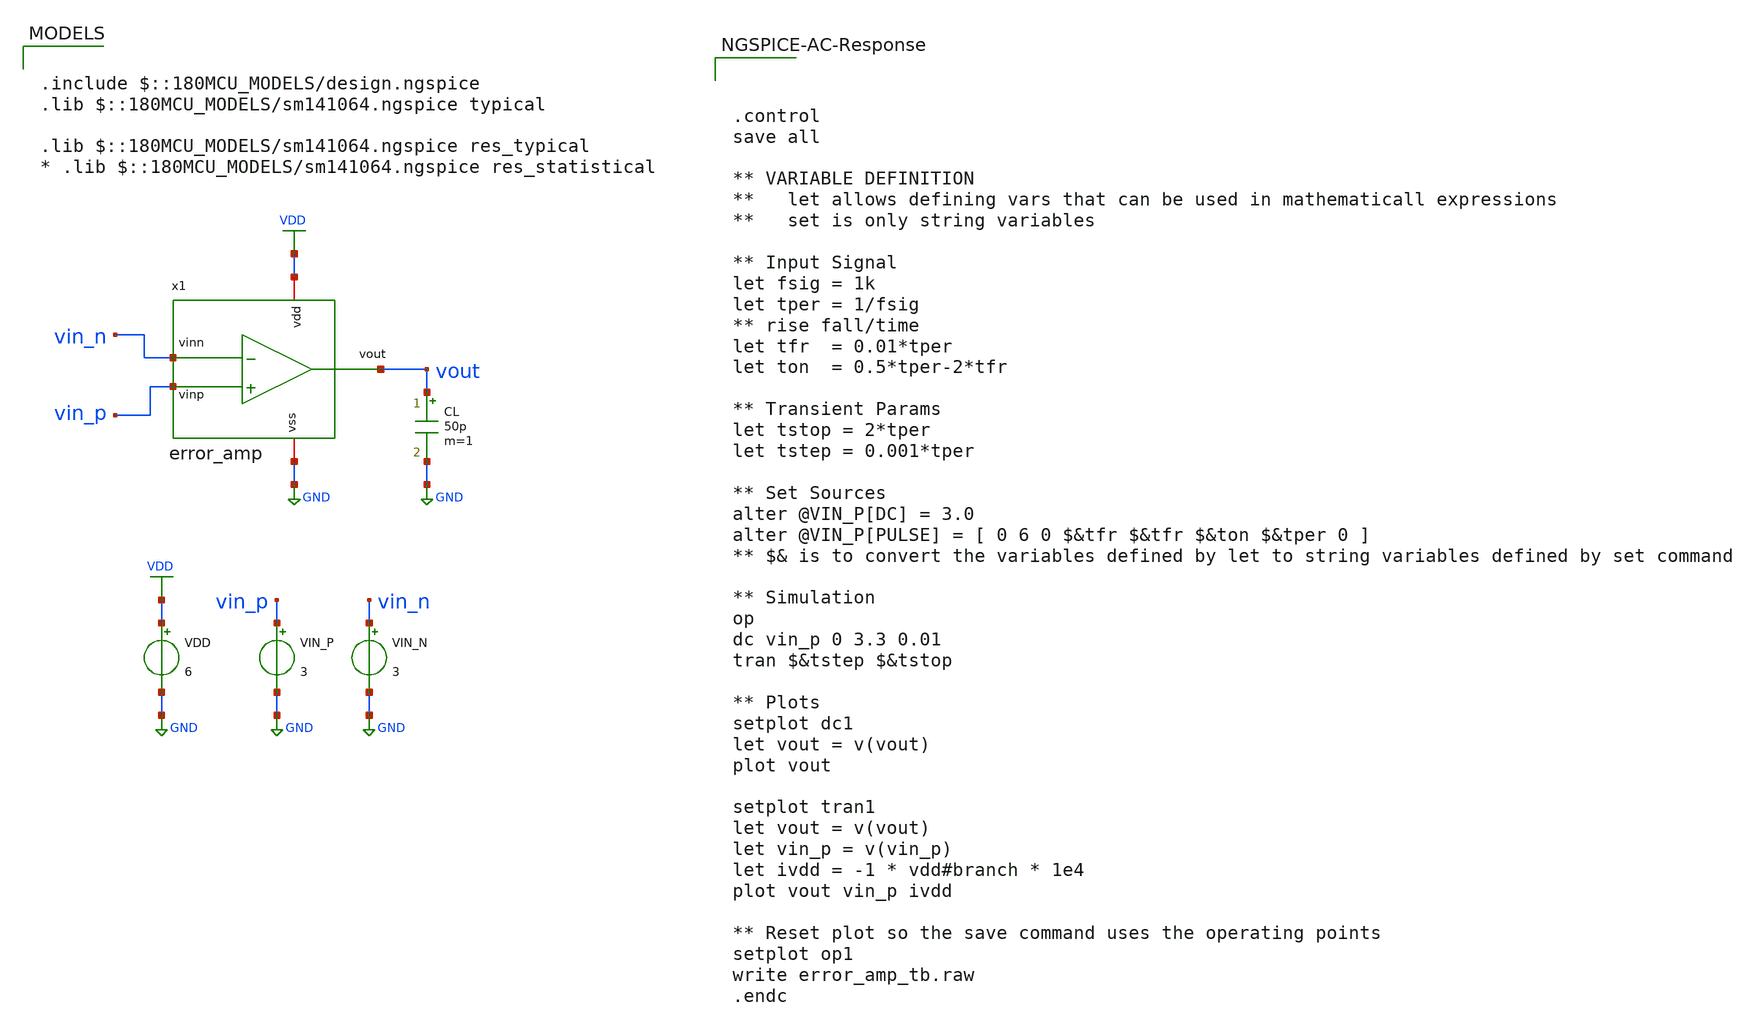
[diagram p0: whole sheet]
** sch_path: analog-db/drawings/ldo-005-ti-ldo-buffer-ref/gf180/error_amp/error_amp_tb.sch
**.subckt error_amp_tb
VDD VDD GND 6
VIN_P vin_p GND 3
VIN_N vin_n GND 3
CL vout GND 50p m=1
x1 VDD vout vin_p vin_n GND error_amp
**** begin user architecture code

.include $::180MCU_MODELS/design.ngspice
.lib $::180MCU_MODELS/sm141064.ngspice typical

.lib $::180MCU_MODELS/sm141064.ngspice res_typical
* .lib $::180MCU_MODELS/sm141064.ngspice res_statistical




.control
save all

** VARIABLE DEFINITION
**   let allows defining vars that can be used in mathematicall expressions
**   set is only string variables

** Input Signal
let fsig = 1k
let tper = 1/fsig
** rise fall/time
let tfr  = 0.01*tper
let ton  = 0.5*tper-2*tfr

** Transient Params
let tstop = 2*tper
let tstep = 0.001*tper

** Set Sources
alter @VIN_P[DC] = 3.0
alter @VIN_P[PULSE] = [ 0 6 0 $&tfr $&tfr $&ton $&tper 0 ]
** $& is to convert the variables defined by let to string variables defined by set command

** Simulation
op
dc vin_p 0 3.3 0.01
tran $&tstep $&tstop

** Plots
setplot dc1
let vout = v(vout)
plot vout

setplot tran1
let vout = v(vout)
let vin_p = v(vin_p)
let ivdd = -1 * vdd#branch * 1e4
plot vout vin_p ivdd

** Reset plot so the save command uses the operating points
setplot op1
write error_amp_tb.raw
.endc





.control
save all

** VARIABLE DEFINITION
**   let allows defining vars that can be used in mathematicall expressions
**   set is only string variables

** Input Signal
let fsig = 1k
let tper = 1/fsig
** rise fall/time
let tfr  = 0.01*tper
let ton  = 0.5*tper-2*tfr

** Transient Params
let tstop = 2*tper
let tstep = 0.001*tper

** Set Sources
alter @VIN_P[DC] = 3.0
alter @VIN_P[PULSE] = [ 0 6 0 $&tfr $&tfr $&ton $&tper 0 ]
** $& is to convert the variables defined by let to string variables defined by set command

** Simulation
op
dc vin_p 0 3.3 0.01
tran $&tstep $&tstop

** Plots
setplot dc1
let vout = v(vout)
plot vout

setplot tran1
let vout = v(vout)
let vin_p = v(vin_p)
let ivdd = -1 * vdd#branch * 1e4
plot vout vin_p ivdd

** Reset plot so the save command uses the operating points
setplot op1
write error_amp_tb.raw
.endc


**** end user architecture code
**.ends

* expanding   symbol:  ldo-005-ti-ldo-buffer-ref/gf180/error_amp/error_amp.sym # of pins=5
** sym_path: analog-db/circuits/amp_032_ti_ldo_error_selfbias/pdk/gf180mcu/schematic/error_amp.sym
** sch_path: analog-db/circuits/amp_032_ti_ldo_error_selfbias/pdk/gf180mcu/schematic/error_amp.sch
.subckt error_amp vdd vout vinp vinn vss
*.iopin vdd
*.iopin vss
*.ipin vinp
*.opin vout
*.ipin vinn
XM2 net_b vinp net_c vss nfet_06v0 L=0.7u W=68.542u nf=1 ad='int((nf+1)/2) * W/nf * 0.18u' as='int((nf+2)/2) * W/nf * 0.18u'
+ pd='2*int((nf+1)/2) * (W/nf + 0.18u)' ps='2*int((nf+2)/2) * (W/nf + 0.18u)' nrd='0.18u / W' nrs='0.18u / W'
+ sa=0 sb=0 sd=0 m=1
XM3m net_a net_d vdd vdd pfet_06v0 L=0.5u W=69.545u nf=1 ad='int((nf+1)/2) * W/nf * 0.18u' as='int((nf+2)/2) * W/nf * 0.18u'
+ pd='2*int((nf+1)/2) * (W/nf + 0.18u)' ps='2*int((nf+2)/2) * (W/nf + 0.18u)' nrd='0.18u / W' nrs='0.18u / W'
+ sa=0 sb=0 sd=0 m=1
XM4 net_f net_a net_d vdd pfet_06v0 L=0.5u W=10u nf=1 ad='int((nf+1)/2) * W/nf * 0.18u' as='int((nf+2)/2) * W/nf * 0.18u'
+ pd='2*int((nf+1)/2) * (W/nf + 0.18u)' ps='2*int((nf+2)/2) * (W/nf + 0.18u)' nrd='0.18u / W' nrs='0.18u / W'
+ sa=0 sb=0 sd=0 m=1
XM5 net_b net_d vdd vdd pfet_06v0 L=0.5u W=69.545u nf=1 ad='int((nf+1)/2) * W/nf * 0.18u' as='int((nf+2)/2) * W/nf * 0.18u'
+ pd='2*int((nf+1)/2) * (W/nf + 0.18u)' ps='2*int((nf+2)/2) * (W/nf + 0.18u)' nrd='0.18u / W' nrs='0.18u / W'
+ sa=0 sb=0 sd=0 m=1
XM6 vout net_b vdd vdd pfet_06v0 L=3.8349u W=20u nf=1 ad='int((nf+1)/2) * W/nf * 0.18u' as='int((nf+2)/2) * W/nf * 0.18u'
+ pd='2*int((nf+1)/2) * (W/nf + 0.18u)' ps='2*int((nf+2)/2) * (W/nf + 0.18u)' nrd='0.18u / W' nrs='0.18u / W'
+ sa=0 sb=0 sd=0 m=1
Cc net1 vout 6.7168p m=1
XRZ net_b net1 vdd ppolyf_u_3k r_width=1u r_length=9.476u m=1
XM1 net_a vinn net_c vss nfet_06v0 L=0.7u W=68.542u nf=1 ad='int((nf+1)/2) * W/nf * 0.18u' as='int((nf+2)/2) * W/nf * 0.18u'
+ pd='2*int((nf+1)/2) * (W/nf + 0.18u)' ps='2*int((nf+2)/2) * (W/nf + 0.18u)' nrd='0.18u / W' nrs='0.18u / W'
+ sa=0 sb=0 sd=0 m=1
XM_mirror_error_amp_ref net2 net2 vss vss nfet_06v0 L=2u W=34.533u nf=1 ad='int((nf+1)/2) * W/nf * 0.18u'
+ as='int((nf+2)/2) * W/nf * 0.18u' pd='2*int((nf+1)/2) * (W/nf + 0.18u)' ps='2*int((nf+2)/2) * (W/nf + 0.18u)'
+ nrd='0.18u / W' nrs='0.18u / W' sa=0 sb=0 sd=0 m=1
XM_mirror_f net_f net2 vss vss nfet_06v0 L=2u W=5u nf=1 ad='int((nf+1)/2) * W/nf * 0.18u' as='int((nf+2)/2) * W/nf * 0.18u'
+ pd='2*int((nf+1)/2) * (W/nf + 0.18u)' ps='2*int((nf+2)/2) * (W/nf + 0.18u)' nrd='0.18u / W' nrs='0.18u / W'
+ sa=0 sb=0 sd=0 m=1
XM_mirror_c net_c net2 vss vss nfet_06v0 L=2u W=34.533u nf=1 ad='int((nf+1)/2) * W/nf * 0.18u' as='int((nf+2)/2) * W/nf * 0.18u'
+ pd='2*int((nf+1)/2) * (W/nf + 0.18u)' ps='2*int((nf+2)/2) * (W/nf + 0.18u)' nrd='0.18u / W' nrs='0.18u / W'
+ sa=0 sb=0 sd=0 m=1
XM_mirror_ea_out vout net2 vss vss nfet_06v0 L=2u W=34.533u nf=1 ad='int((nf+1)/2) * W/nf * 0.18u' as='int((nf+2)/2) * W/nf * 0.18u'
+ pd='2*int((nf+1)/2) * (W/nf + 0.18u)' ps='2*int((nf+2)/2) * (W/nf + 0.18u)' nrd='0.18u / W' nrs='0.18u / W'
+ sa=0 sb=0 sd=0 m=1
XM_bias net2 net2 vdd vdd pfet_06v0 L=2u W=6.3111u nf=1 ad='int((nf+1)/2) * W/nf * 0.18u' as='int((nf+2)/2) * W/nf * 0.18u'
+ pd='2*int((nf+1)/2) * (W/nf + 0.18u)' ps='2*int((nf+2)/2) * (W/nf + 0.18u)' nrd='0.18u / W' nrs='0.18u / W'
+ sa=0 sb=0 sd=0 m=1
.ends

.GLOBAL VDD
.GLOBAL GND
.end
